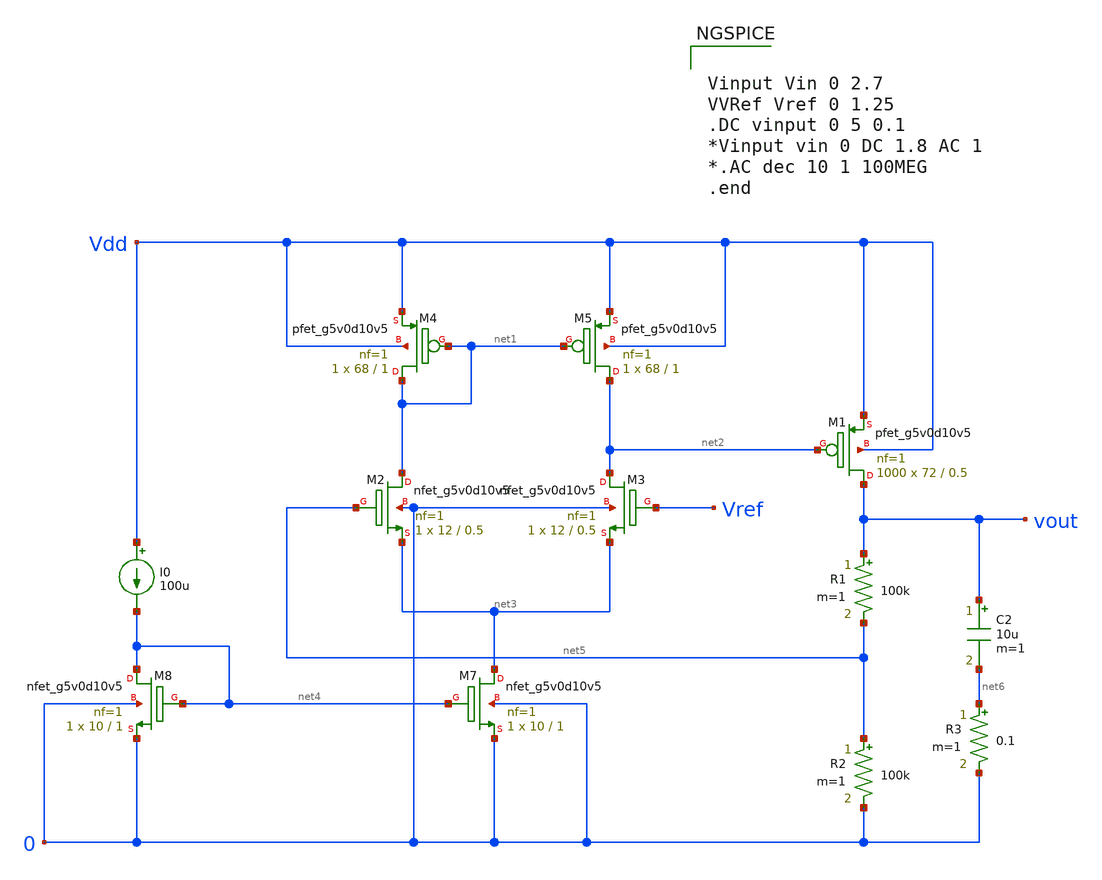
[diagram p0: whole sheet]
** sch_path: LDO/Schematic/LDO_5TOTA.sch
**.subckt LDO_5TOTA
I0 Vdd net4 100u
XM2 net1 net5 net3 0 sky130_fd_pr__nfet_g5v0d10v5 L=0.5 W=12 nf=1 ad='int((nf+1)/2) * W/nf * 0.29' as='int((nf+2)/2) * W/nf * 0.29'
+ pd='2*int((nf+1)/2) * (W/nf + 0.29)' ps='2*int((nf+2)/2) * (W/nf + 0.29)' nrd='0.29 / W' nrs='0.29 / W'
+ sa=0 sb=0 sd=0 mult=1 m=1
XM3 net2 Vref net3 0 sky130_fd_pr__nfet_g5v0d10v5 L=0.5 W=12 nf=1 ad='int((nf+1)/2) * W/nf * 0.29' as='int((nf+2)/2) * W/nf * 0.29'
+ pd='2*int((nf+1)/2) * (W/nf + 0.29)' ps='2*int((nf+2)/2) * (W/nf + 0.29)' nrd='0.29 / W' nrs='0.29 / W'
+ sa=0 sb=0 sd=0 mult=1 m=1
XM4 net1 net1 Vdd Vdd sky130_fd_pr__pfet_g5v0d10v5 L=1 W=68 nf=1 ad='int((nf+1)/2) * W/nf * 0.29' as='int((nf+2)/2) * W/nf * 0.29'
+ pd='2*int((nf+1)/2) * (W/nf + 0.29)' ps='2*int((nf+2)/2) * (W/nf + 0.29)' nrd='0.29 / W' nrs='0.29 / W'
+ sa=0 sb=0 sd=0 mult=1 m=1
XM5 net2 net1 Vdd Vdd sky130_fd_pr__pfet_g5v0d10v5 L=1 W=68 nf=1 ad='int((nf+1)/2) * W/nf * 0.29' as='int((nf+2)/2) * W/nf * 0.29'
+ pd='2*int((nf+1)/2) * (W/nf + 0.29)' ps='2*int((nf+2)/2) * (W/nf + 0.29)' nrd='0.29 / W' nrs='0.29 / W'
+ sa=0 sb=0 sd=0 mult=1 m=1
XM7 net3 net4 0 0 sky130_fd_pr__nfet_g5v0d10v5 L=1 W=10 nf=1 ad='int((nf+1)/2) * W/nf * 0.29' as='int((nf+2)/2) * W/nf * 0.29'
+ pd='2*int((nf+1)/2) * (W/nf + 0.29)' ps='2*int((nf+2)/2) * (W/nf + 0.29)' nrd='0.29 / W' nrs='0.29 / W'
+ sa=0 sb=0 sd=0 mult=1 m=1
XM8 net4 net4 0 0 sky130_fd_pr__nfet_g5v0d10v5 L=1 W=10 nf=1 ad='int((nf+1)/2) * W/nf * 0.29' as='int((nf+2)/2) * W/nf * 0.29'
+ pd='2*int((nf+1)/2) * (W/nf + 0.29)' ps='2*int((nf+2)/2) * (W/nf + 0.29)' nrd='0.29 / W' nrs='0.29 / W'
+ sa=0 sb=0 sd=0 mult=1 m=1
R1 vout net5 100k m=1
R2 net5 0 100k m=1
XM1 vout net2 Vdd Vdd sky130_fd_pr__pfet_g5v0d10v5 L=0.5 W=72 nf=1 ad='int((nf+1)/2) * W/nf * 0.29' as='int((nf+2)/2) * W/nf * 0.29'
+ pd='2*int((nf+1)/2) * (W/nf + 0.29)' ps='2*int((nf+2)/2) * (W/nf + 0.29)' nrd='0.29 / W' nrs='0.29 / W'
+ sa=0 sb=0 sd=0 mult=1000 m=1000
C2 vout net6 10u m=1
R3 net6 0 0.1 m=1
**** begin user architecture code


Vinput Vin 0 2.7
VVRef Vref 0 1.25
.DC vinput 0 5 0.1
*Vinput vin 0 DC 1.8 AC 1
*.AC dec 10 1 100MEG
.end



.include $::SKYWATER_MODELS/cells/nfet_01v8/sky130_fd_pr__nfet_01v8__tt.corner.spice
.include $::SKYWATER_MODELS/cells/nfet_01v8_lvt/sky130_fd_pr__nfet_01v8_lvt__tt.corner.spice
.include $::SKYWATER_MODELS/cells/pfet_01v8/sky130_fd_pr__pfet_01v8__tt.corner.spice
.include $::SKYWATER_MODELS/cells/nfet_03v3_nvt/sky130_fd_pr__nfet_03v3_nvt__tt.corner.spice
.include $::SKYWATER_MODELS/cells/nfet_05v0_nvt/sky130_fd_pr__nfet_05v0_nvt__tt.corner.spice
.include $::SKYWATER_MODELS/cells/esd_nfet_01v8/sky130_fd_pr__esd_nfet_01v8__tt.corner.spice
.include $::SKYWATER_MODELS/cells/pfet_01v8_lvt/sky130_fd_pr__pfet_01v8_lvt__tt.corner.spice
.include $::SKYWATER_MODELS/cells/pfet_01v8_hvt/sky130_fd_pr__pfet_01v8_hvt__tt.corner.spice
.include $::SKYWATER_MODELS/cells/esd_pfet_g5v0d10v5/sky130_fd_pr__esd_pfet_g5v0d10v5__tt.corner.spice
.include $::SKYWATER_MODELS/cells/pfet_g5v0d10v5/sky130_fd_pr__pfet_g5v0d10v5__tt.corner.spice
.include $::SKYWATER_MODELS/cells/pfet_g5v0d16v0/sky130_fd_pr__pfet_g5v0d16v0__tt.corner.spice
.include $::SKYWATER_MODELS/cells/nfet_g5v0d10v5/sky130_fd_pr__nfet_g5v0d10v5__tt.corner.spice
.include $::SKYWATER_MODELS/cells/nfet_g5v0d16v0/sky130_fd_pr__nfet_g5v0d16v0__tt_discrete.corner.spice
.include $::SKYWATER_MODELS/cells/esd_nfet_g5v0d10v5/sky130_fd_pr__esd_nfet_g5v0d10v5__tt.corner.spice
.include $::SKYWATER_MODELS/models/corners/tt/nonfet.spice
* Mismatch parameters
.include $::SKYWATER_MODELS/cells/nfet_01v8/sky130_fd_pr__nfet_01v8__mismatch.corner.spice
.include $::SKYWATER_MODELS/cells/pfet_01v8/sky130_fd_pr__pfet_01v8__mismatch.corner.spice
.include $::SKYWATER_MODELS/cells/nfet_01v8_lvt/sky130_fd_pr__nfet_01v8_lvt__mismatch.corner.spice
.include $::SKYWATER_MODELS/cells/pfet_01v8_lvt/sky130_fd_pr__pfet_01v8_lvt__mismatch.corner.spice
.include $::SKYWATER_MODELS/cells/pfet_01v8_hvt/sky130_fd_pr__pfet_01v8_hvt__mismatch.corner.spice
.include $::SKYWATER_MODELS/cells/nfet_g5v0d10v5/sky130_fd_pr__nfet_g5v0d10v5__mismatch.corner.spice
.include $::SKYWATER_MODELS/cells/pfet_g5v0d10v5/sky130_fd_pr__pfet_g5v0d10v5__mismatch.corner.spice
.include $::SKYWATER_MODELS/cells/nfet_05v0_nvt/sky130_fd_pr__nfet_05v0_nvt__mismatch.corner.spice
.include $::SKYWATER_MODELS/cells/nfet_03v3_nvt/sky130_fd_pr__nfet_03v3_nvt__mismatch.corner.spice
* Resistor$::SKYWATER_MODELS/Capacitor
.include $::SKYWATER_MODELS/models/r+c/res_typical__cap_typical.spice
.include $::SKYWATER_MODELS/models/r+c/res_typical__cap_typical__lin.spice
* Special cells
.include $::SKYWATER_MODELS/models/corners/tt/specialized_cells.spice
* All models
.include $::SKYWATER_MODELS/models/all.spice
* Corner
.include $::SKYWATER_MODELS/models/corners/tt/rf.spice

**** end user architecture code
**.ends
.end
